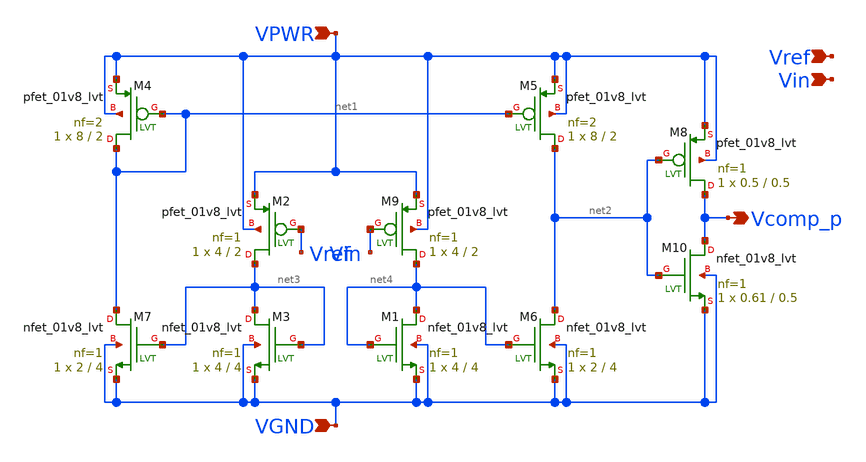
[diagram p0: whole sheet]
** sch_path: xschem/subckts/PComp.sch
**.subckt PComp Vcomp_p Vref Vin VPWR VGND
*.opin Vcomp_p
*.ipin Vref
*.ipin Vin
*.ipin VPWR
*.ipin VGND
XM1 net4 net4 VGND VGND sky130_fd_pr__nfet_01v8_lvt L=4 W=4 nf=1 ad='int((nf+1)/2) * W/nf * 0.29' as='int((nf+2)/2) * W/nf * 0.29'
+ pd='2*int((nf+1)/2) * (W/nf + 0.29)' ps='2*int((nf+2)/2) * (W/nf + 0.29)' nrd='0.29 / W' nrs='0.29 / W'
+ sa=0 sb=0 sd=0 mult=1 m=1
XM3 net3 net3 VGND VGND sky130_fd_pr__nfet_01v8_lvt L=4 W=4 nf=1 ad='int((nf+1)/2) * W/nf * 0.29' as='int((nf+2)/2) * W/nf * 0.29'
+ pd='2*int((nf+1)/2) * (W/nf + 0.29)' ps='2*int((nf+2)/2) * (W/nf + 0.29)' nrd='0.29 / W' nrs='0.29 / W'
+ sa=0 sb=0 sd=0 mult=1 m=1
XM9 net4 Vin VPWR VPWR sky130_fd_pr__pfet_01v8_lvt L=2 W=4 nf=1 ad='int((nf+1)/2) * W/nf * 0.29' as='int((nf+2)/2) * W/nf * 0.29'
+ pd='2*int((nf+1)/2) * (W/nf + 0.29)' ps='2*int((nf+2)/2) * (W/nf + 0.29)' nrd='0.29 / W' nrs='0.29 / W'
+ sa=0 sb=0 sd=0 mult=1 m=1
XM2 net3 Vref VPWR VPWR sky130_fd_pr__pfet_01v8_lvt L=2 W=4 nf=1 ad='int((nf+1)/2) * W/nf * 0.29' as='int((nf+2)/2) * W/nf * 0.29'
+ pd='2*int((nf+1)/2) * (W/nf + 0.29)' ps='2*int((nf+2)/2) * (W/nf + 0.29)' nrd='0.29 / W' nrs='0.29 / W'
+ sa=0 sb=0 sd=0 mult=1 m=1
XM4 net1 net1 VPWR VPWR sky130_fd_pr__pfet_01v8_lvt L=2 W=8 nf=2 ad='int((nf+1)/2) * W/nf * 0.29' as='int((nf+2)/2) * W/nf * 0.29'
+ pd='2*int((nf+1)/2) * (W/nf + 0.29)' ps='2*int((nf+2)/2) * (W/nf + 0.29)' nrd='0.29 / W' nrs='0.29 / W'
+ sa=0 sb=0 sd=0 mult=1 m=1
XM5 net2 net1 VPWR VPWR sky130_fd_pr__pfet_01v8_lvt L=2 W=8 nf=2 ad='int((nf+1)/2) * W/nf * 0.29' as='int((nf+2)/2) * W/nf * 0.29'
+ pd='2*int((nf+1)/2) * (W/nf + 0.29)' ps='2*int((nf+2)/2) * (W/nf + 0.29)' nrd='0.29 / W' nrs='0.29 / W'
+ sa=0 sb=0 sd=0 mult=1 m=1
XM6 net2 net4 VGND VGND sky130_fd_pr__nfet_01v8_lvt L=4 W=2 nf=1 ad='int((nf+1)/2) * W/nf * 0.29' as='int((nf+2)/2) * W/nf * 0.29'
+ pd='2*int((nf+1)/2) * (W/nf + 0.29)' ps='2*int((nf+2)/2) * (W/nf + 0.29)' nrd='0.29 / W' nrs='0.29 / W'
+ sa=0 sb=0 sd=0 mult=1 m=1
XM7 net1 net3 VGND VGND sky130_fd_pr__nfet_01v8_lvt L=4 W=2 nf=1 ad='int((nf+1)/2) * W/nf * 0.29' as='int((nf+2)/2) * W/nf * 0.29'
+ pd='2*int((nf+1)/2) * (W/nf + 0.29)' ps='2*int((nf+2)/2) * (W/nf + 0.29)' nrd='0.29 / W' nrs='0.29 / W'
+ sa=0 sb=0 sd=0 mult=1 m=1
XM8 Vcomp_p net2 VPWR VPWR sky130_fd_pr__pfet_01v8_lvt L=0.5 W=0.5 nf=1 ad='int((nf+1)/2) * W/nf * 0.29'
+ as='int((nf+2)/2) * W/nf * 0.29' pd='2*int((nf+1)/2) * (W/nf + 0.29)' ps='2*int((nf+2)/2) * (W/nf + 0.29)'
+ nrd='0.29 / W' nrs='0.29 / W' sa=0 sb=0 sd=0 mult=1 m=1
XM10 Vcomp_p net2 VGND VGND sky130_fd_pr__nfet_01v8_lvt L=0.5 W=0.61 nf=1 ad='int((nf+1)/2) * W/nf * 0.29'
+ as='int((nf+2)/2) * W/nf * 0.29' pd='2*int((nf+1)/2) * (W/nf + 0.29)' ps='2*int((nf+2)/2) * (W/nf + 0.29)'
+ nrd='0.29 / W' nrs='0.29 / W' sa=0 sb=0 sd=0 mult=1 m=1
**.ends
.end
